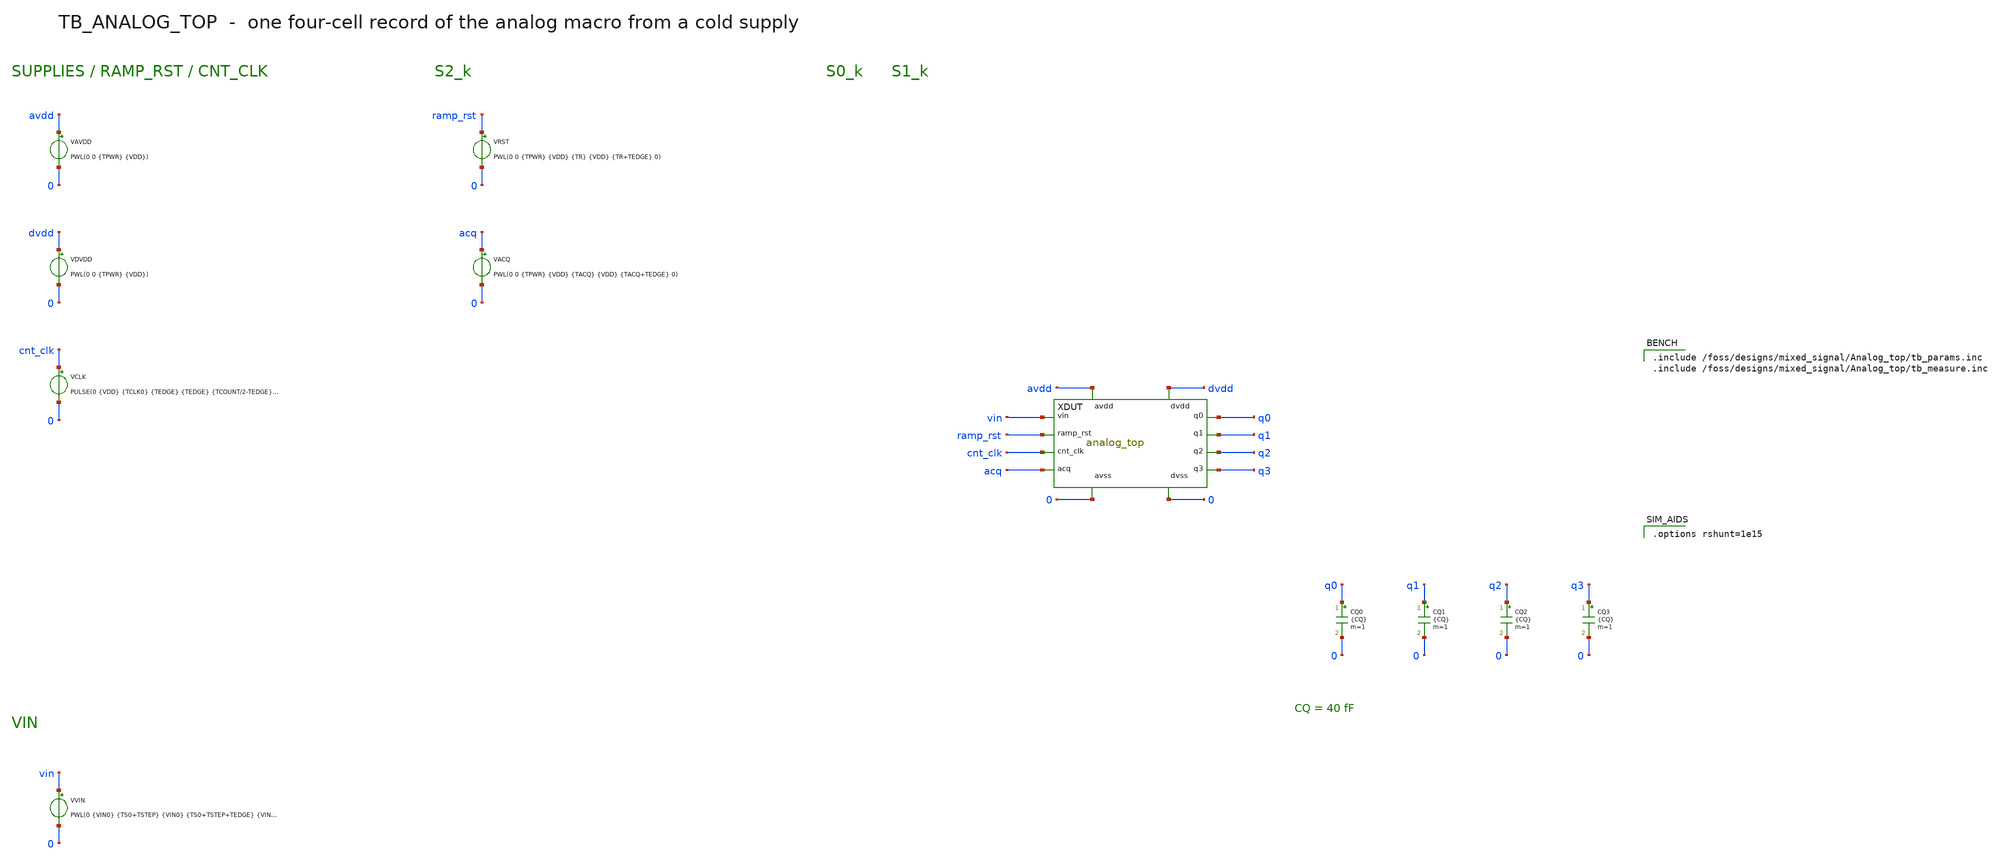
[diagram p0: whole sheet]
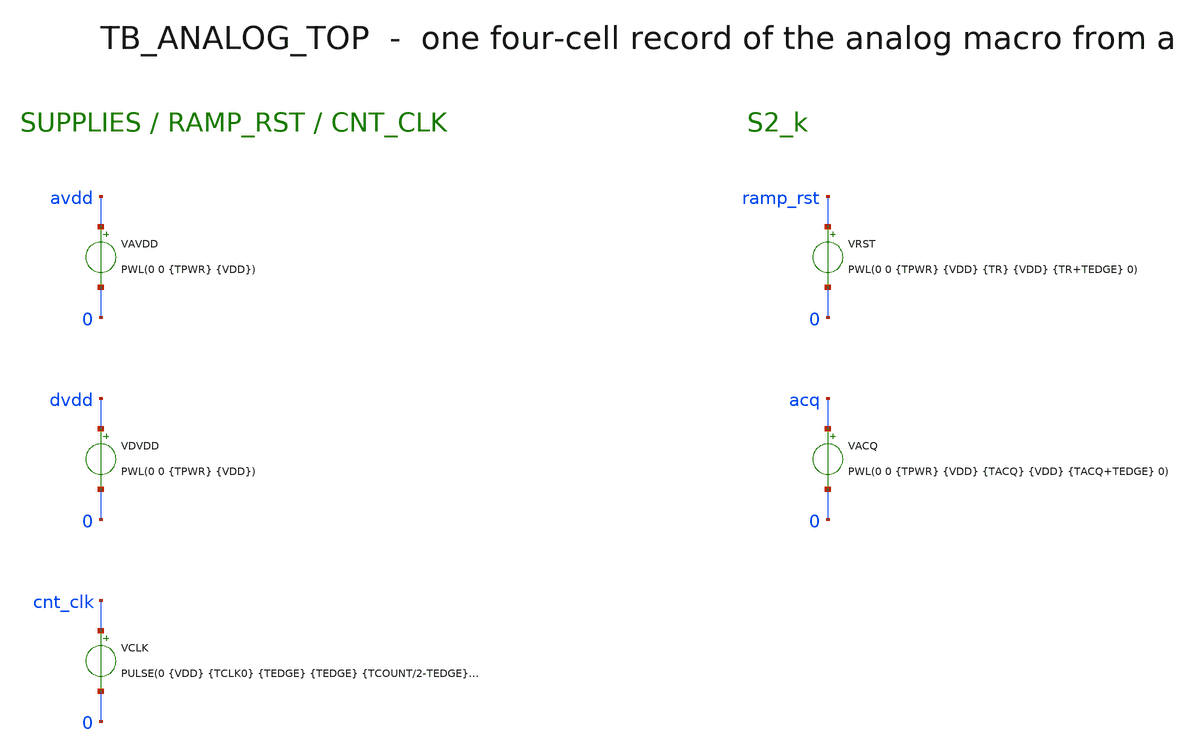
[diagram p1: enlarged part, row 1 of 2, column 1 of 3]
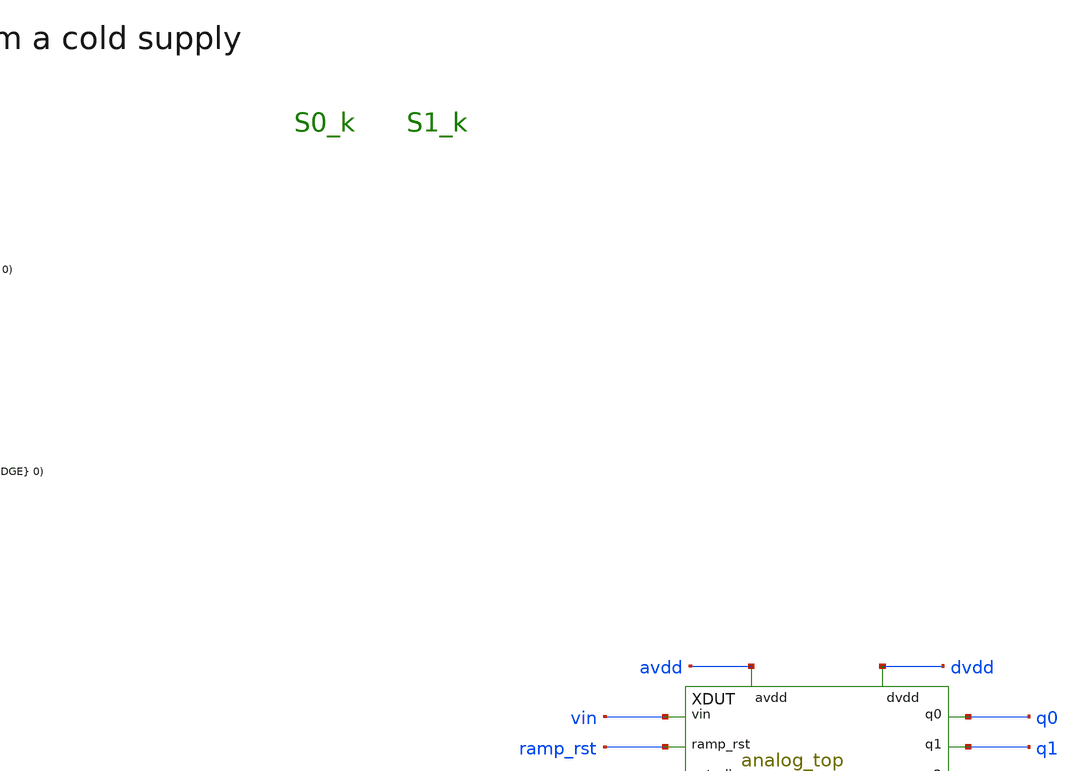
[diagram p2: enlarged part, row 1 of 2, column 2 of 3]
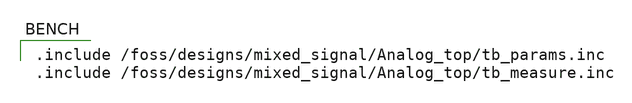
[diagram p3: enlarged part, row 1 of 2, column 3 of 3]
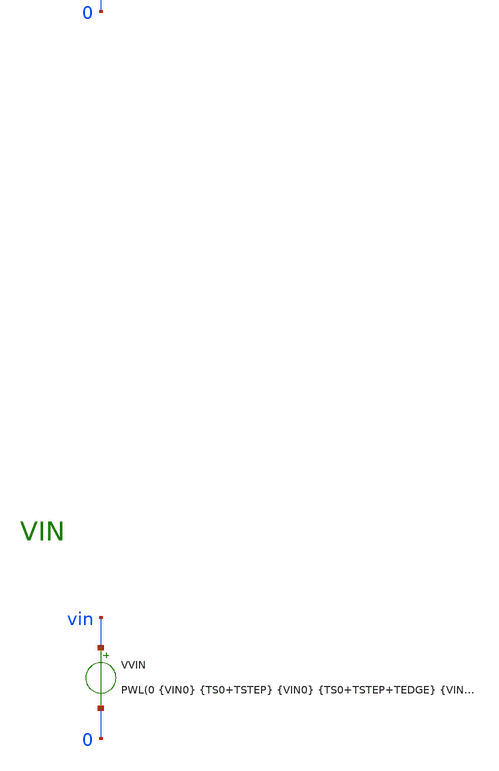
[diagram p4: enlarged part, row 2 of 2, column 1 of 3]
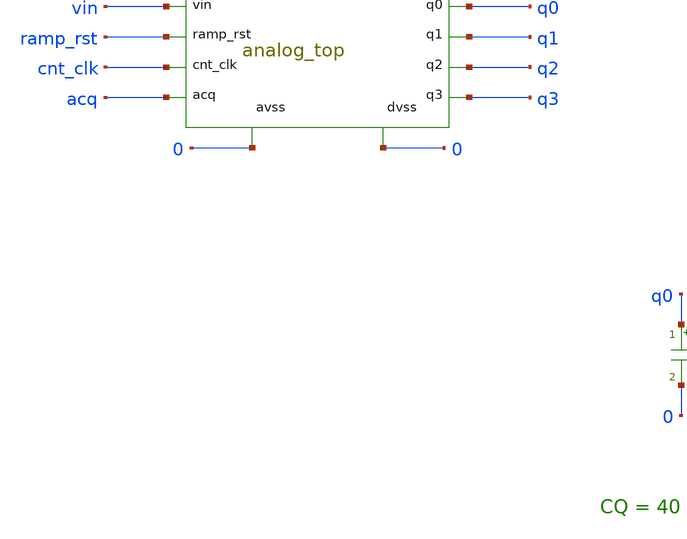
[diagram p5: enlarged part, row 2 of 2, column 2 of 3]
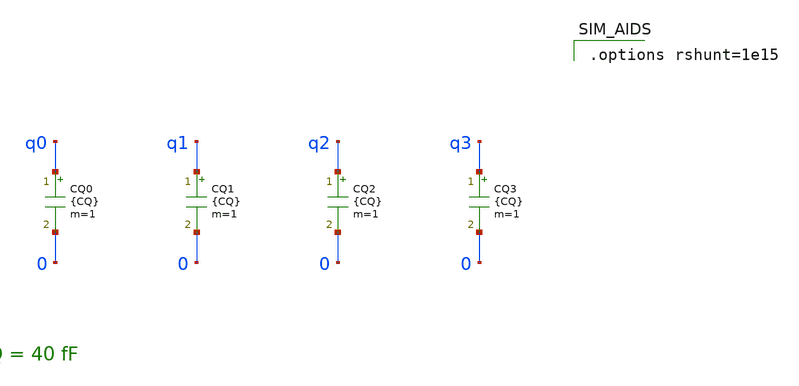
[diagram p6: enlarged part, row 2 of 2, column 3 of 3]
** sch_path: mixed_signal/Analog_top/tb_analog_top.sch
**.subckt tb_analog_top
VAVDD avdd 0 PWL(0 0 {TPWR} {VDD})
VDVDD dvdd 0 PWL(0 0 {TPWR} {VDD})
VCLK cnt_clk 0 PULSE(0 {VDD} {TCLK0} {TEDGE} {TEDGE} {TCOUNT/2-TEDGE} {TCOUNT})
VRST ramp_rst 0 PWL(0 0 {TPWR} {VDD} {TR} {VDD} {TR+TEDGE} 0)
VACQ acq 0 PWL(0 0 {TPWR} {VDD} {TACQ} {VDD} {TACQ+TEDGE} 0)
VVIN vin 0 PWL(0 {VIN0} {TS0+TSTEP} {VIN0} {TS0+TSTEP+TEDGE} {VIN1} {TS1+TSTEP} {VIN1} {TS1+TSTEP+TEDGE}
+ {VIN2} {TS2+TSTEP} {VIN2} {TS2+TSTEP+TEDGE} {VIN3})
XDUT vin ramp_rst cnt_clk acq q0 q1 q2 q3 avdd 0 dvdd 0 analog_top
CQ0 q0 0 {CQ} m=1
CQ1 q1 0 {CQ} m=1
CQ2 q2 0 {CQ} m=1
CQ3 q3 0 {CQ} m=1
**** begin user architecture code

.include /foss/pdks/gf180mcuD/libs.tech/ngspice/design.ngspice
.lib /foss/pdks/gf180mcuD/libs.tech/ngspice/sm141064.ngspice typical
.lib /foss/pdks/gf180mcuD/libs.tech/ngspice/sm141064.ngspice res_typical
.lib /foss/pdks/gf180mcuD/libs.tech/ngspice/sm141064.ngspice mimcap_typical
.include /foss/pdk_libs/gf180mcuD/libs.ref/gf180mcu_as_sc_mcu7t3v3/spice/gf180mcu_as_sc_mcu7t3v3.spice


.include /foss/designs/mixed_signal/Analog_top/tb_params.inc
.include /foss/designs/mixed_signal/Analog_top/tb_measure.inc


.options rshunt=1e15

**** end user architecture code
**.ends
.end
